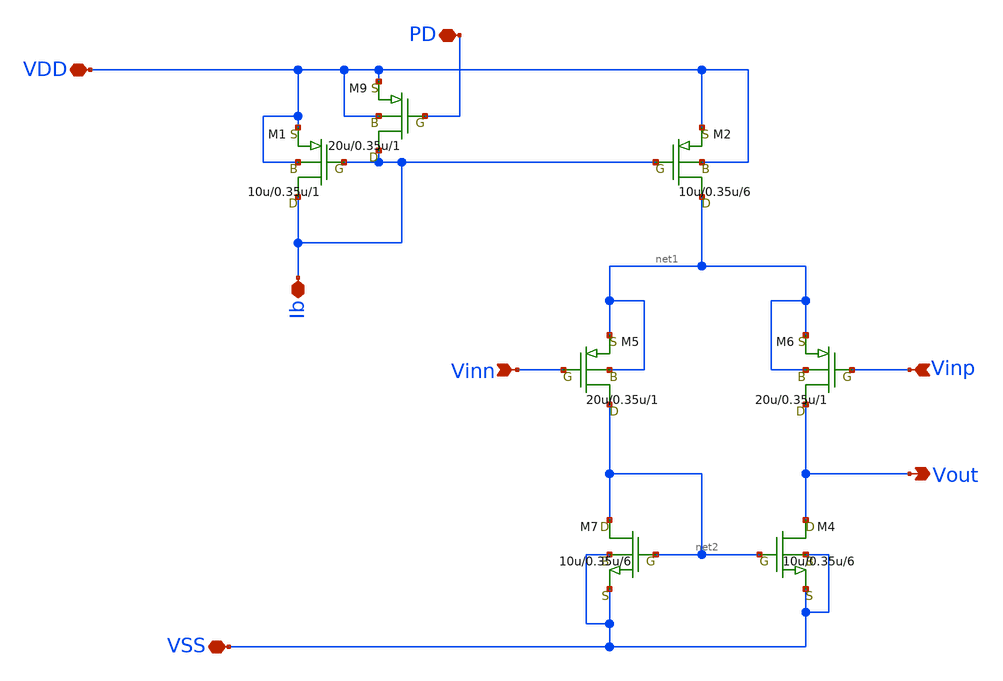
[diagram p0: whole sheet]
** sch_path: OPAmpPforRTR.sch
**.subckt OPAmpPforRTR Vout Vinn Vinp Ib VDD VSS PD
*.opin Vout
*.ipin Vinn
*.ipin Vinp
*.iopin Ib
*.iopin VDD
*.iopin VSS
*.iopin PD
M1 Ib Ib VDD VDD pch w=10u l=0.35u as=0 ps=0 ad=0 pd=0 m=1
M2 net1 Ib VDD VDD pch w=10u l=0.35u as=0 ps=0 ad=0 pd=0 m=6
M4 Vout net2 VSS VSS nch w=10u l=0.35u as=0 ps=0 ad=0 pd=0 m=6
M5 net2 Vinn net1 net1 pch w=20u l=0.35u as=0 ps=0 ad=0 pd=0 m=1
M6 Vout Vinp net1 net1 pch w=20u l=0.35u as=0 ps=0 ad=0 pd=0 m=1
M7 net2 net2 VSS VSS nch w=10u l=0.35u as=0 ps=0 ad=0 pd=0 m=6
M9 Ib PD VDD VDD pch w=20u l=0.35u as=0 ps=0 ad=0 pd=0 m=1
**.ends
.end
